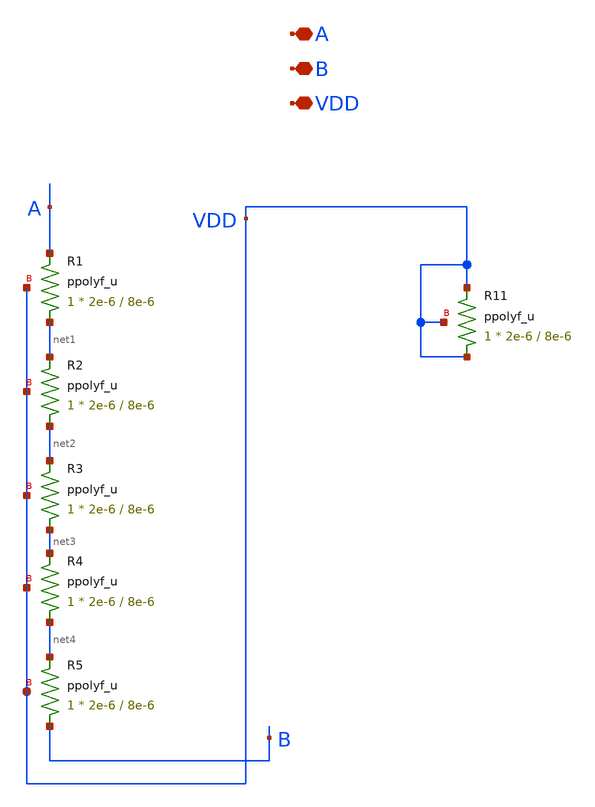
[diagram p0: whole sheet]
** sch_path: SCOP_INPUT_AND_MUX_PAKISTAN_03/Xschem/TransImpedance/resis_7_5k.sch
**.subckt resis_7_5k A B VDD
*.iopin A
*.iopin B
*.iopin VDD
XR1 net1 A VDD ppolyf_u r_width=2e-6 r_length=8e-6 m=1
XR2 net2 net1 VDD ppolyf_u r_width=2e-6 r_length=8e-6 m=1
XR3 net3 net2 VDD ppolyf_u r_width=2e-6 r_length=8e-6 m=1
XR4 net4 net3 VDD ppolyf_u r_width=2e-6 r_length=8e-6 m=1
XR5 B net4 VDD ppolyf_u r_width=2e-6 r_length=8e-6 m=1
XR11 VDD VDD VDD ppolyf_u r_width=2e-6 r_length=8e-6 m=1
**.ends
.end
